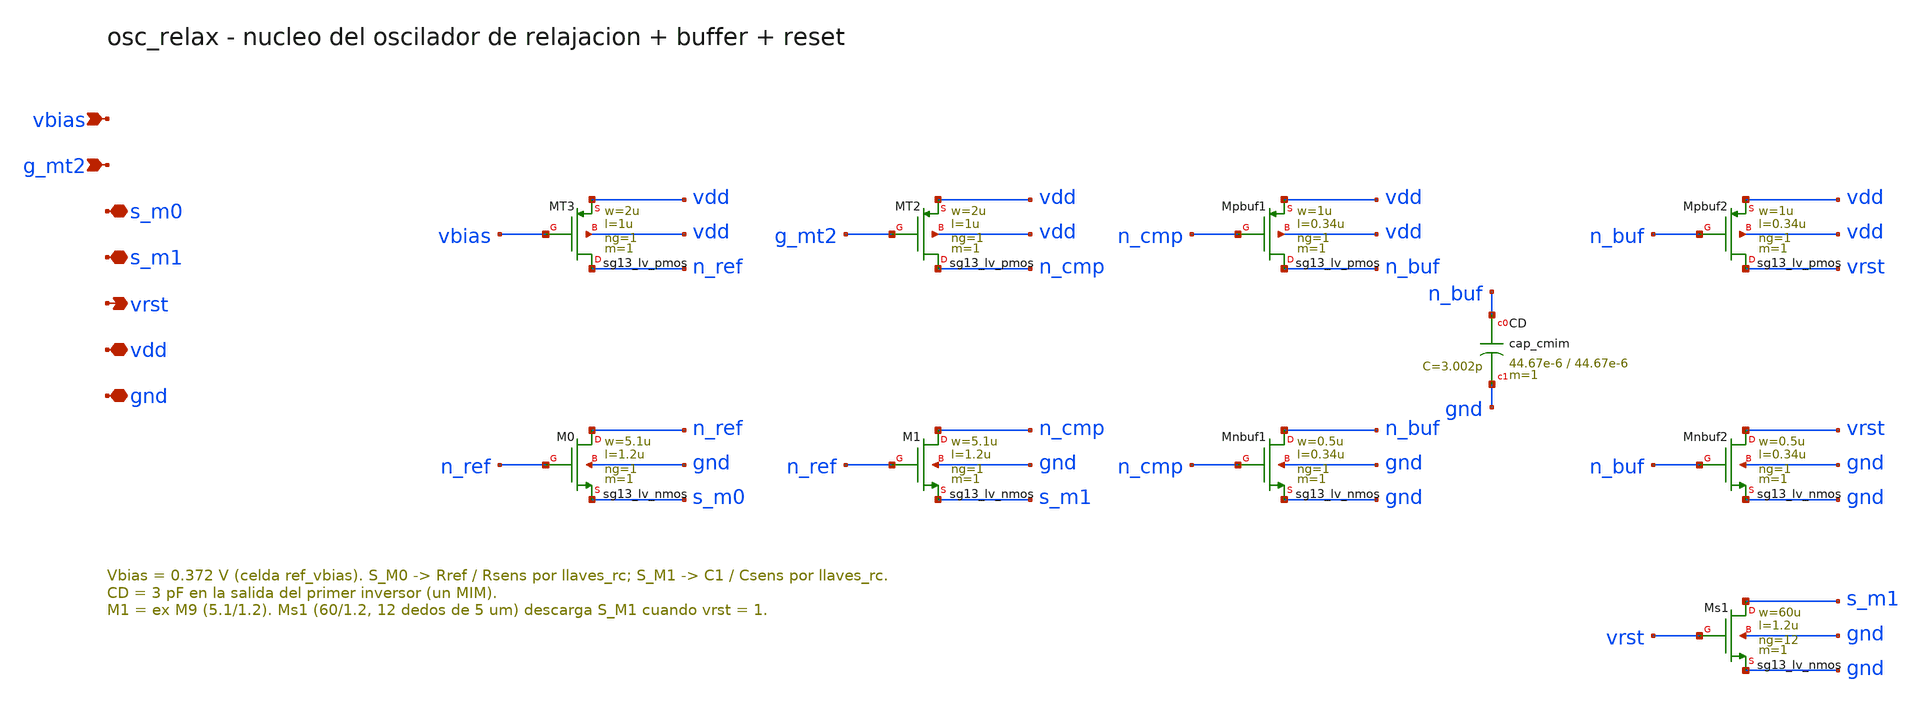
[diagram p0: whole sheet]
** sch_path: Enfoque_B/xschem/celdas/osc_relax.sch
**.subckt osc_relax vbias g_mt2 s_m0 s_m1 vrst vdd gnd
*.ipin vbias
*.ipin g_mt2
*.iopin s_m0
*.iopin s_m1
*.opin vrst
*.iopin vdd
*.iopin gnd
XMT3 n_ref vbias vdd vdd sg13_lv_pmos w=2u l=1u ng=1 m=1 mm_ok=1
XMT2 n_cmp g_mt2 vdd vdd sg13_lv_pmos w=2u l=1u ng=1 m=1 mm_ok=1
XM0 n_ref n_ref s_m0 gnd sg13_lv_nmos w=5.1u l=1.2u ng=1 m=1 mm_ok=1
XM1 n_cmp n_ref s_m1 gnd sg13_lv_nmos w=5.1u l=1.2u ng=1 m=1 mm_ok=1
XMpbuf1 n_buf n_cmp vdd vdd sg13_lv_pmos w=1u l=0.34u ng=1 m=1 mm_ok=1
XMnbuf1 n_buf n_cmp gnd gnd sg13_lv_nmos w=0.5u l=0.34u ng=1 m=1 mm_ok=1
XCD n_buf gnd cap_cmim w=44.67e-6 l=44.67e-6 m=1 mm_ok=1
XMpbuf2 vrst n_buf vdd vdd sg13_lv_pmos w=1u l=0.34u ng=1 m=1 mm_ok=1
XMnbuf2 vrst n_buf gnd gnd sg13_lv_nmos w=0.5u l=0.34u ng=1 m=1 mm_ok=1
XMs1 s_m1 vrst gnd gnd sg13_lv_nmos w=60u l=1.2u ng=12 m=1 mm_ok=1
**.ends
.end
